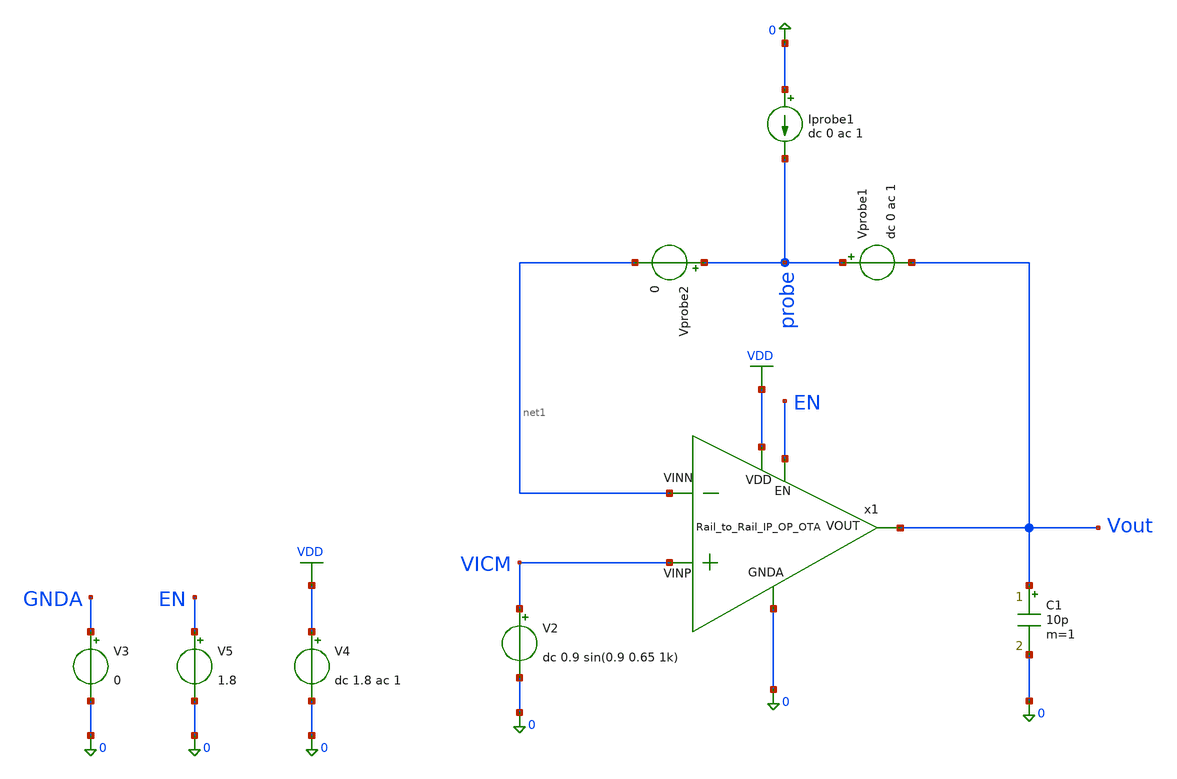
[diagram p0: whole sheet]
** sch_path: OTAs/Rail_to_Rail_IP_OP_SWING_OTA__IP/SCH/Rail_to_Rail_IP_OP_OTA_STB.sch
.lib $::SKYWATER_MODELS/sky130.lib.spice tt
.include $::SKYWATER_STDCELLS/sky130_fd_sc_hd.spice

**.subckt Rail_to_Rail_IP_OP_OTA_STB
V3 GNDA 0 0
V5 EN 0 1.8
C1 Vout 0 10p m=1
Vprobe1 probe Vout dc 0 ac 1
Vprobe2 probe net1 0
Iprobe1 0 probe dc 0 ac 1
x1 VDD VICM net1 Vout EN 0 Rail_to_Rail_IP_OP_OTA
V2 VICM 0 dc 0.9 sin(0.9 0.65 1k)
V4 VDD 0 dc 1.8 ac 1
**** begin user architecture code



.save @m.x1.xmn_bot_l2.msky130_fd_pr__nfet_01v8[gm]
.save @m.x1.xmn_bot_l2.msky130_fd_pr__nfet_01v8[gds]
.save @m.x1.xmn_bot_l2.msky130_fd_pr__nfet_01v8[vth]
.save @m.x1.xmn_bot_l2.msky130_fd_pr__nfet_01v8[vdsat]
.save @m.x1.xmn_bot_l2.msky130_fd_pr__nfet_01v8[cgg]
.save @m.x1.xmn_bot_l2.msky130_fd_pr__nfet_01v8[cgso]
.save @m.x1.xmn_bot_l2.msky130_fd_pr__nfet_01v8[cgdo]
.save @m.x1.xmn_casc_l2.msky130_fd_pr__nfet_01v8[gm]
.save @m.x1.xmn_casc_l2.msky130_fd_pr__nfet_01v8[gds]
.save @m.x1.xmn_casc_l2.msky130_fd_pr__nfet_01v8[vth]
.save @m.x1.xmn_casc_l2.msky130_fd_pr__nfet_01v8[vdsat]
.save @m.x1.xmn_casc_l2.msky130_fd_pr__nfet_01v8[cgg]
.save @m.x1.xmn_casc_l2.msky130_fd_pr__nfet_01v8[cgso]
.save @m.x1.xmn_casc_l2.msky130_fd_pr__nfet_01v8[cgdo]
.save @m.x1.xmn_bot_l1.msky130_fd_pr__nfet_01v8[gm]
.save @m.x1.xmn_bot_l1.msky130_fd_pr__nfet_01v8[gds]
.save @m.x1.xmn_bot_l1.msky130_fd_pr__nfet_01v8[vth]
.save @m.x1.xmn_bot_l1.msky130_fd_pr__nfet_01v8[vdsat]
.save @m.x1.xmn_bot_l1.msky130_fd_pr__nfet_01v8[cgg]
.save @m.x1.xmn_bot_l1.msky130_fd_pr__nfet_01v8[cgso]
.save @m.x1.xmn_bot_l1.msky130_fd_pr__nfet_01v8[cgdo]
.save @m.x1.xmn_casc_l1.msky130_fd_pr__nfet_01v8[gm]
.save @m.x1.xmn_casc_l1.msky130_fd_pr__nfet_01v8[gds]
.save @m.x1.xmn_casc_l1.msky130_fd_pr__nfet_01v8[vth]
.save @m.x1.xmn_casc_l1.msky130_fd_pr__nfet_01v8[vdsat]
.save @m.x1.xmn_casc_l1.msky130_fd_pr__nfet_01v8[cgg]
.save @m.x1.xmn_casc_l1.msky130_fd_pr__nfet_01v8[cgso]
.save @m.x1.xmn_casc_l1.msky130_fd_pr__nfet_01v8[cgdo]
.save @m.x1.xmp_casc_l2.msky130_fd_pr__pfet_01v8[gm]
.save @m.x1.xmp_casc_l2.msky130_fd_pr__pfet_01v8[gds]
.save @m.x1.xmp_casc_l2.msky130_fd_pr__pfet_01v8[vth]
.save @m.x1.xmp_casc_l2.msky130_fd_pr__pfet_01v8[vdsat]
.save @m.x1.xmp_casc_l2.msky130_fd_pr__pfet_01v8[cgg]
.save @m.x1.xmp_casc_l2.msky130_fd_pr__pfet_01v8[cgso]
.save @m.x1.xmp_casc_l2.msky130_fd_pr__pfet_01v8[cgdo]
.save @m.x1.xmp_casc_l1.msky130_fd_pr__pfet_01v8[gm]
.save @m.x1.xmp_casc_l1.msky130_fd_pr__pfet_01v8[gds]
.save @m.x1.xmp_casc_l1.msky130_fd_pr__pfet_01v8[vth]
.save @m.x1.xmp_casc_l1.msky130_fd_pr__pfet_01v8[vdsat]
.save @m.x1.xmp_casc_l1.msky130_fd_pr__pfet_01v8[cgg]
.save @m.x1.xmp_casc_l1.msky130_fd_pr__pfet_01v8[cgso]
.save @m.x1.xmp_casc_l1.msky130_fd_pr__pfet_01v8[cgdo]
.save @m.x1.xmp_top_l1.msky130_fd_pr__pfet_01v8[gm]
.save @m.x1.xmp_top_l1.msky130_fd_pr__pfet_01v8[gds]
.save @m.x1.xmp_top_l1.msky130_fd_pr__pfet_01v8[vth]
.save @m.x1.xmp_top_l1.msky130_fd_pr__pfet_01v8[vdsat]
.save @m.x1.xmp_top_l1.msky130_fd_pr__pfet_01v8[cgg]
.save @m.x1.xmp_top_l1.msky130_fd_pr__pfet_01v8[cgso]
.save @m.x1.xmp_top_l1.msky130_fd_pr__pfet_01v8[cgdo]
.save @m.x1.xmn_a1.msky130_fd_pr__nfet_01v8_lvt[gm]
.save @m.x1.xmn_a1.msky130_fd_pr__nfet_01v8_lvt[gds]
.save @m.x1.xmn_a1.msky130_fd_pr__nfet_01v8_lvt[vth]
.save @m.x1.xmn_a1.msky130_fd_pr__nfet_01v8_lvt[vdsat]
.save @m.x1.xmn_a1.msky130_fd_pr__nfet_01v8_lvt[cgg]
.save @m.x1.xmn_a1.msky130_fd_pr__nfet_01v8_lvt[cgso]
.save @m.x1.xmn_a1.msky130_fd_pr__nfet_01v8_lvt[cgdo]
.save @m.x1.xmn_a2.msky130_fd_pr__nfet_01v8_lvt[gm]
.save @m.x1.xmn_a2.msky130_fd_pr__nfet_01v8_lvt[gds]
.save @m.x1.xmn_a2.msky130_fd_pr__nfet_01v8_lvt[vth]
.save @m.x1.xmn_a2.msky130_fd_pr__nfet_01v8_lvt[vdsat]
.save @m.x1.xmn_a2.msky130_fd_pr__nfet_01v8_lvt[cgg]
.save @m.x1.xmn_a2.msky130_fd_pr__nfet_01v8_lvt[cgso]
.save @m.x1.xmn_a2.msky130_fd_pr__nfet_01v8_lvt[cgdo]
.save @m.x1.xmp_a1.msky130_fd_pr__pfet_01v8_lvt[gm]
.save @m.x1.xmp_a1.msky130_fd_pr__pfet_01v8_lvt[gds]
.save @m.x1.xmp_a1.msky130_fd_pr__pfet_01v8_lvt[vth]
.save @m.x1.xmp_a1.msky130_fd_pr__pfet_01v8_lvt[vdsat]
.save @m.x1.xmp_a1.msky130_fd_pr__pfet_01v8_lvt[cgg]
.save @m.x1.xmp_a1.msky130_fd_pr__pfet_01v8_lvt[cgso]
.save @m.x1.xmp_a1.msky130_fd_pr__pfet_01v8_lvt[cgdo]
.save @m.x1.xmp_a2.msky130_fd_pr__pfet_01v8_lvt[gm]
.save @m.x1.xmp_a2.msky130_fd_pr__pfet_01v8_lvt[gds]
.save @m.x1.xmp_a2.msky130_fd_pr__pfet_01v8_lvt[vth]
.save @m.x1.xmp_a2.msky130_fd_pr__pfet_01v8_lvt[vdsat]
.save @m.x1.xmp_a2.msky130_fd_pr__pfet_01v8_lvt[cgg]
.save @m.x1.xmp_a2.msky130_fd_pr__pfet_01v8_lvt[cgso]
.save @m.x1.xmp_a2.msky130_fd_pr__pfet_01v8_lvt[cgdo]
.save @m.x1.xmp_pdiff_bias.msky130_fd_pr__pfet_01v8[gm]
.save @m.x1.xmp_pdiff_bias.msky130_fd_pr__pfet_01v8[gds]
.save @m.x1.xmp_pdiff_bias.msky130_fd_pr__pfet_01v8[vth]
.save @m.x1.xmp_pdiff_bias.msky130_fd_pr__pfet_01v8[vdsat]
.save @m.x1.xmp_pdiff_bias.msky130_fd_pr__pfet_01v8[cgg]
.save @m.x1.xmp_pdiff_bias.msky130_fd_pr__pfet_01v8[cgso]
.save @m.x1.xmp_pdiff_bias.msky130_fd_pr__pfet_01v8[cgdo]
.save @m.x1.xmn_ndiff_bias.msky130_fd_pr__nfet_01v8[gm]
.save @m.x1.xmn_ndiff_bias.msky130_fd_pr__nfet_01v8[gds]
.save @m.x1.xmn_ndiff_bias.msky130_fd_pr__nfet_01v8[vth]
.save @m.x1.xmn_ndiff_bias.msky130_fd_pr__nfet_01v8[vdsat]
.save @m.x1.xmn_ndiff_bias.msky130_fd_pr__nfet_01v8[cgg]
.save @m.x1.xmn_ndiff_bias.msky130_fd_pr__nfet_01v8[cgso]
.save @m.x1.xmn_ndiff_bias.msky130_fd_pr__nfet_01v8[cgdo]
.save @m.x1.xmp_pdiff_bias_b.msky130_fd_pr__pfet_01v8[gm]
.save @m.x1.xmp_pdiff_bias_b.msky130_fd_pr__pfet_01v8[gds]
.save @m.x1.xmp_pdiff_bias_b.msky130_fd_pr__pfet_01v8[vth]
.save @m.x1.xmp_pdiff_bias_b.msky130_fd_pr__pfet_01v8[vdsat]
.save @m.x1.xmp_pdiff_bias_b.msky130_fd_pr__pfet_01v8[cgg]
.save @m.x1.xmp_pdiff_bias_b.msky130_fd_pr__pfet_01v8[cgso]
.save @m.x1.xmp_pdiff_bias_b.msky130_fd_pr__pfet_01v8[cgdo]
.save @m.x1.xmp_top_l2.msky130_fd_pr__pfet_01v8[gm]
.save @m.x1.xmp_top_l2.msky130_fd_pr__pfet_01v8[gds]
.save @m.x1.xmp_top_l2.msky130_fd_pr__pfet_01v8[vth]
.save @m.x1.xmp_top_l2.msky130_fd_pr__pfet_01v8[vdsat]
.save @m.x1.xmp_top_l2.msky130_fd_pr__pfet_01v8[cgg]
.save @m.x1.xmp_top_l2.msky130_fd_pr__pfet_01v8[cgso]
.save @m.x1.xmp_top_l2.msky130_fd_pr__pfet_01v8[cgdo]
.save @m.x1.xmn_bias_source.msky130_fd_pr__nfet_01v8[gm]
.save @m.x1.xmn_bias_source.msky130_fd_pr__nfet_01v8[gds]
.save @m.x1.xmn_bias_source.msky130_fd_pr__nfet_01v8[vth]
.save @m.x1.xmn_bias_source.msky130_fd_pr__nfet_01v8[vdsat]
.save @m.x1.xmn_bias_source.msky130_fd_pr__nfet_01v8[cgg]
.save @m.x1.xmn_bias_source.msky130_fd_pr__nfet_01v8[cgso]
.save @m.x1.xmn_bias_source.msky130_fd_pr__nfet_01v8[cgdo]
.save @m.x1.xmn_bias_ext.msky130_fd_pr__nfet_01v8[gm]
.save @m.x1.xmn_bias_ext.msky130_fd_pr__nfet_01v8[gds]
.save @m.x1.xmn_bias_ext.msky130_fd_pr__nfet_01v8[vth]
.save @m.x1.xmn_bias_ext.msky130_fd_pr__nfet_01v8[vdsat]
.save @m.x1.xmn_bias_ext.msky130_fd_pr__nfet_01v8[cgg]
.save @m.x1.xmn_bias_ext.msky130_fd_pr__nfet_01v8[cgso]
.save @m.x1.xmn_bias_ext.msky130_fd_pr__nfet_01v8[cgdo]
.save @m.x1.xmp_casc_b_source.msky130_fd_pr__pfet_01v8[gm]
.save @m.x1.xmp_casc_b_source.msky130_fd_pr__pfet_01v8[gds]
.save @m.x1.xmp_casc_b_source.msky130_fd_pr__pfet_01v8[vth]
.save @m.x1.xmp_casc_b_source.msky130_fd_pr__pfet_01v8[vdsat]
.save @m.x1.xmp_casc_b_source.msky130_fd_pr__pfet_01v8[cgg]
.save @m.x1.xmp_casc_b_source.msky130_fd_pr__pfet_01v8[cgso]
.save @m.x1.xmp_casc_b_source.msky130_fd_pr__pfet_01v8[cgdo]
.save @m.x1.xmn_casc_bias8.msky130_fd_pr__nfet_01v8[gm]
.save @m.x1.xmn_casc_bias8.msky130_fd_pr__nfet_01v8[gds]
.save @m.x1.xmn_casc_bias8.msky130_fd_pr__nfet_01v8[vth]
.save @m.x1.xmn_casc_bias8.msky130_fd_pr__nfet_01v8[vdsat]
.save @m.x1.xmn_casc_bias8.msky130_fd_pr__nfet_01v8[cgg]
.save @m.x1.xmn_casc_bias8.msky130_fd_pr__nfet_01v8[cgso]
.save @m.x1.xmn_casc_bias8.msky130_fd_pr__nfet_01v8[cgdo]
.save @m.x1.xmn_casc_b_source.msky130_fd_pr__nfet_01v8[gm]
.save @m.x1.xmn_casc_b_source.msky130_fd_pr__nfet_01v8[gds]
.save @m.x1.xmn_casc_b_source.msky130_fd_pr__nfet_01v8[vth]
.save @m.x1.xmn_casc_b_source.msky130_fd_pr__nfet_01v8[vdsat]
.save @m.x1.xmn_casc_b_source.msky130_fd_pr__nfet_01v8[cgg]
.save @m.x1.xmn_casc_b_source.msky130_fd_pr__nfet_01v8[cgso]
.save @m.x1.xmn_casc_b_source.msky130_fd_pr__nfet_01v8[cgdo]
.save @m.x1.xmp_casc_bias1.msky130_fd_pr__pfet_01v8[gm]
.save @m.x1.xmp_casc_bias1.msky130_fd_pr__pfet_01v8[gds]
.save @m.x1.xmp_casc_bias1.msky130_fd_pr__pfet_01v8[vth]
.save @m.x1.xmp_casc_bias1.msky130_fd_pr__pfet_01v8[vdsat]
.save @m.x1.xmp_casc_bias1.msky130_fd_pr__pfet_01v8[cgg]
.save @m.x1.xmp_casc_bias1.msky130_fd_pr__pfet_01v8[cgso]
.save @m.x1.xmp_casc_bias1.msky130_fd_pr__pfet_01v8[cgdo]
.save @m.x1.xmn_casc_bias7.msky130_fd_pr__nfet_01v8[gm]
.save @m.x1.xmn_casc_bias7.msky130_fd_pr__nfet_01v8[gds]
.save @m.x1.xmn_casc_bias7.msky130_fd_pr__nfet_01v8[vth]
.save @m.x1.xmn_casc_bias7.msky130_fd_pr__nfet_01v8[vdsat]
.save @m.x1.xmn_casc_bias7.msky130_fd_pr__nfet_01v8[cgg]
.save @m.x1.xmn_casc_bias7.msky130_fd_pr__nfet_01v8[cgso]
.save @m.x1.xmn_casc_bias7.msky130_fd_pr__nfet_01v8[cgdo]
.save @m.x1.xmn_casc_bias6.msky130_fd_pr__nfet_01v8[gm]
.save @m.x1.xmn_casc_bias6.msky130_fd_pr__nfet_01v8[gds]
.save @m.x1.xmn_casc_bias6.msky130_fd_pr__nfet_01v8[vth]
.save @m.x1.xmn_casc_bias6.msky130_fd_pr__nfet_01v8[vdsat]
.save @m.x1.xmn_casc_bias6.msky130_fd_pr__nfet_01v8[cgg]
.save @m.x1.xmn_casc_bias6.msky130_fd_pr__nfet_01v8[cgso]
.save @m.x1.xmn_casc_bias6.msky130_fd_pr__nfet_01v8[cgdo]
.save @m.x1.xmp_casc_bias2.msky130_fd_pr__pfet_01v8[gm]
.save @m.x1.xmp_casc_bias2.msky130_fd_pr__pfet_01v8[gds]
.save @m.x1.xmp_casc_bias2.msky130_fd_pr__pfet_01v8[vth]
.save @m.x1.xmp_casc_bias2.msky130_fd_pr__pfet_01v8[vdsat]
.save @m.x1.xmp_casc_bias2.msky130_fd_pr__pfet_01v8[cgg]
.save @m.x1.xmp_casc_bias2.msky130_fd_pr__pfet_01v8[cgso]
.save @m.x1.xmp_casc_bias2.msky130_fd_pr__pfet_01v8[cgdo]
.save @m.x1.xmp_casc_bias3.msky130_fd_pr__pfet_01v8[gm]
.save @m.x1.xmp_casc_bias3.msky130_fd_pr__pfet_01v8[gds]
.save @m.x1.xmp_casc_bias3.msky130_fd_pr__pfet_01v8[vth]
.save @m.x1.xmp_casc_bias3.msky130_fd_pr__pfet_01v8[vdsat]
.save @m.x1.xmp_casc_bias3.msky130_fd_pr__pfet_01v8[cgg]
.save @m.x1.xmp_casc_bias3.msky130_fd_pr__pfet_01v8[cgso]
.save @m.x1.xmp_casc_bias3.msky130_fd_pr__pfet_01v8[cgdo]
.save @m.x1.xmn_casc_bias5.msky130_fd_pr__nfet_01v8[gm]
.save @m.x1.xmn_casc_bias5.msky130_fd_pr__nfet_01v8[gds]
.save @m.x1.xmn_casc_bias5.msky130_fd_pr__nfet_01v8[vth]
.save @m.x1.xmn_casc_bias5.msky130_fd_pr__nfet_01v8[vdsat]
.save @m.x1.xmn_casc_bias5.msky130_fd_pr__nfet_01v8[cgg]
.save @m.x1.xmn_casc_bias5.msky130_fd_pr__nfet_01v8[cgso]
.save @m.x1.xmn_casc_bias5.msky130_fd_pr__nfet_01v8[cgdo]
.save @m.x1.xmn_casc_bias4.msky130_fd_pr__nfet_01v8[gm]
.save @m.x1.xmn_casc_bias4.msky130_fd_pr__nfet_01v8[gds]
.save @m.x1.xmn_casc_bias4.msky130_fd_pr__nfet_01v8[vth]
.save @m.x1.xmn_casc_bias4.msky130_fd_pr__nfet_01v8[vdsat]
.save @m.x1.xmn_casc_bias4.msky130_fd_pr__nfet_01v8[cgg]
.save @m.x1.xmn_casc_bias4.msky130_fd_pr__nfet_01v8[cgso]
.save @m.x1.xmn_casc_bias4.msky130_fd_pr__nfet_01v8[cgdo]
.save @m.x1.xmn_casc_bias3.msky130_fd_pr__nfet_01v8[gm]
.save @m.x1.xmn_casc_bias3.msky130_fd_pr__nfet_01v8[gds]
.save @m.x1.xmn_casc_bias3.msky130_fd_pr__nfet_01v8[vth]
.save @m.x1.xmn_casc_bias3.msky130_fd_pr__nfet_01v8[vdsat]
.save @m.x1.xmn_casc_bias3.msky130_fd_pr__nfet_01v8[cgg]
.save @m.x1.xmn_casc_bias3.msky130_fd_pr__nfet_01v8[cgso]
.save @m.x1.xmn_casc_bias3.msky130_fd_pr__nfet_01v8[cgdo]
.save @m.x1.xmn_casc_bias1.msky130_fd_pr__nfet_01v8[gm]
.save @m.x1.xmn_casc_bias1.msky130_fd_pr__nfet_01v8[gds]
.save @m.x1.xmn_casc_bias1.msky130_fd_pr__nfet_01v8[vth]
.save @m.x1.xmn_casc_bias1.msky130_fd_pr__nfet_01v8[vdsat]
.save @m.x1.xmn_casc_bias1.msky130_fd_pr__nfet_01v8[cgg]
.save @m.x1.xmn_casc_bias1.msky130_fd_pr__nfet_01v8[cgso]
.save @m.x1.xmn_casc_bias1.msky130_fd_pr__nfet_01v8[cgdo]
.save @m.x1.xmn_casc_bias2.msky130_fd_pr__nfet_01v8[gm]
.save @m.x1.xmn_casc_bias2.msky130_fd_pr__nfet_01v8[gds]
.save @m.x1.xmn_casc_bias2.msky130_fd_pr__nfet_01v8[vth]
.save @m.x1.xmn_casc_bias2.msky130_fd_pr__nfet_01v8[vdsat]
.save @m.x1.xmn_casc_bias2.msky130_fd_pr__nfet_01v8[cgg]
.save @m.x1.xmn_casc_bias2.msky130_fd_pr__nfet_01v8[cgso]
.save @m.x1.xmn_casc_bias2.msky130_fd_pr__nfet_01v8[cgdo]
.save @m.x1.xmn_sw1.msky130_fd_pr__nfet_01v8[gm]
.save @m.x1.xmn_sw1.msky130_fd_pr__nfet_01v8[gds]
.save @m.x1.xmn_sw1.msky130_fd_pr__nfet_01v8[vth]
.save @m.x1.xmn_sw1.msky130_fd_pr__nfet_01v8[vdsat]
.save @m.x1.xmn_sw1.msky130_fd_pr__nfet_01v8[cgg]
.save @m.x1.xmn_sw1.msky130_fd_pr__nfet_01v8[cgso]
.save @m.x1.xmn_sw1.msky130_fd_pr__nfet_01v8[cgdo]
.save @m.x1.xmp_sw1.msky130_fd_pr__pfet_01v8[gm]
.save @m.x1.xmp_sw1.msky130_fd_pr__pfet_01v8[gds]
.save @m.x1.xmp_sw1.msky130_fd_pr__pfet_01v8[vth]
.save @m.x1.xmp_sw1.msky130_fd_pr__pfet_01v8[vdsat]
.save @m.x1.xmp_sw1.msky130_fd_pr__pfet_01v8[cgg]
.save @m.x1.xmp_sw1.msky130_fd_pr__pfet_01v8[cgso]
.save @m.x1.xmp_sw1.msky130_fd_pr__pfet_01v8[cgdo]
.save @m.x1.xmp_sw2.msky130_fd_pr__pfet_01v8[gm]
.save @m.x1.xmp_sw2.msky130_fd_pr__pfet_01v8[gds]
.save @m.x1.xmp_sw2.msky130_fd_pr__pfet_01v8[vth]
.save @m.x1.xmp_sw2.msky130_fd_pr__pfet_01v8[vdsat]
.save @m.x1.xmp_sw2.msky130_fd_pr__pfet_01v8[cgg]
.save @m.x1.xmp_sw2.msky130_fd_pr__pfet_01v8[cgso]
.save @m.x1.xmp_sw2.msky130_fd_pr__pfet_01v8[cgdo]
.save @m.x1.xmn_sw2.msky130_fd_pr__nfet_01v8[gm]
.save @m.x1.xmn_sw2.msky130_fd_pr__nfet_01v8[gds]
.save @m.x1.xmn_sw2.msky130_fd_pr__nfet_01v8[vth]
.save @m.x1.xmn_sw2.msky130_fd_pr__nfet_01v8[vdsat]
.save @m.x1.xmn_sw2.msky130_fd_pr__nfet_01v8[cgg]
.save @m.x1.xmn_sw2.msky130_fd_pr__nfet_01v8[cgso]
.save @m.x1.xmn_sw2.msky130_fd_pr__nfet_01v8[cgdo]
.save @m.x1.xmp_sw3.msky130_fd_pr__pfet_01v8[gm]
.save @m.x1.xmp_sw3.msky130_fd_pr__pfet_01v8[gds]
.save @m.x1.xmp_sw3.msky130_fd_pr__pfet_01v8[vth]
.save @m.x1.xmp_sw3.msky130_fd_pr__pfet_01v8[vdsat]
.save @m.x1.xmp_sw3.msky130_fd_pr__pfet_01v8[cgg]
.save @m.x1.xmp_sw3.msky130_fd_pr__pfet_01v8[cgso]
.save @m.x1.xmp_sw3.msky130_fd_pr__pfet_01v8[cgdo]




.options savecurrents
.control
 save all
 let runs=2
 let run=0

 alter @Vprobe1[acmag]=1
 alter @iprobe1[acmag]=0

 dowhile run < runs
 set run =”$&run”
 ac dec 20 1 1e8
 write OTA_STB_TB_{$run}.raw
 all
 alter @Vprobe1[acmag]=0
 alter @iprobe1[acmag]=1
 let run = run + 1
 end

 let ip22 = ac2.i(Vprobe2)
 let vprb1 = ac1.probe
 let mb = 1/(vprb1+ip22)-1
 let phase_mb = 180/PI*vp(mb)
 plot vdb(mb)
 plot phase_mb
 plot vdb(mb) phase_mb
 echo -------------------------------
 echo -------------------------------
 meas ac peak MAX vmag(mb) FROM=2 TO=1.5GHZ
 let f3db = peak/sqrt(2)
 meas ac f1 WHEN vmag(mb)=f3db RISE=1
 meas ac BW WHEN vmag(mb)=f3db FALL=1
 let GBW = peak*BW
 meas ac pm_deg find phase_mb when vdb(mb)=0
 meas ac dominant_pole_f when vdb(mb)=0
 meas ac loop_gain find vdb(mb) at=0.01
 print GBW
 op
 **show m : gm : gmbs : gds : vds : vdsat : vgs : vth : id
.endc

**** end user architecture code
**.ends
.GLOBAL VDD
.end
